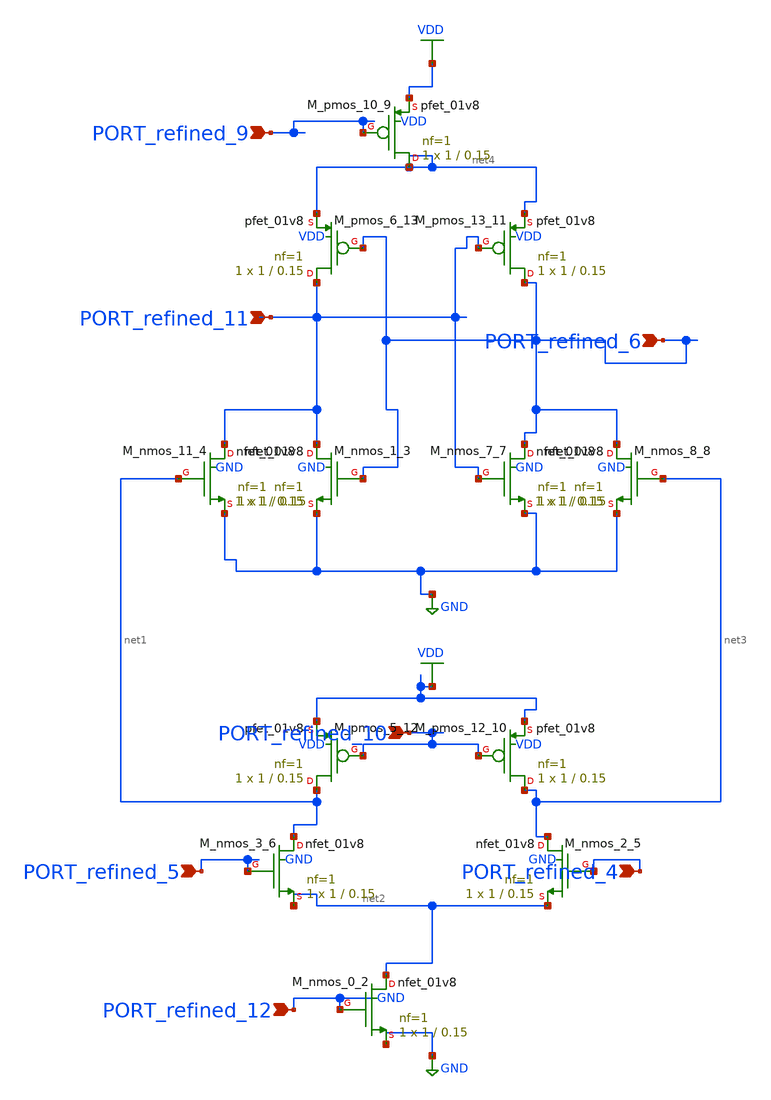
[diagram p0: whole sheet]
** sch_path: schematics/10_1109_ACCESS_2019_2927514_02_002.sch
**.subckt 10_1109_ACCESS_2019_2927514_02_002 PORT_refined_4 PORT_refined_11 PORT_refined_12
*+ PORT_refined_5 PORT_refined_9 PORT_refined_10 PORT_refined_6
*.ipin PORT_refined_4
*.ipin PORT_refined_11
*.ipin PORT_refined_12
*.ipin PORT_refined_5
*.ipin PORT_refined_9
*.ipin PORT_refined_10
*.ipin PORT_refined_6
XM_nmos_0_2 net2 PORT_refined_12 GND GND sky130_fd_pr__nfet_01v8 L=0.15 W=1 nf=1 ad='int((1 + 1)/2) * 1 / 1 * 0.29'
+ as='int((1 + 2)/2) * 1 / 1 * 0.29' pd='2*int((1 + 1)/2) * (1 / 1 + 0.29)' ps='2*int((1 + 2)/2) * (1 / 1 + 0.29)'
+ nrd='0.29 / 1 ' nrs='0.29 / 1 ' sa=0 sb=0 sd=0 mult=1 m=1
XM_nmos_1_3 PORT_refined_11 PORT_refined_6 GND GND sky130_fd_pr__nfet_01v8 L=0.15 W=1 nf=1 ad='int((1 + 1)/2) * 1 / 1 * 0.29'
+ as='int((1 + 2)/2) * 1 / 1 * 0.29' pd='2*int((1 + 1)/2) * (1 / 1 + 0.29)' ps='2*int((1 + 2)/2) * (1 / 1 + 0.29)'
+ nrd='0.29 / 1 ' nrs='0.29 / 1 ' sa=0 sb=0 sd=0 mult=1 m=1
XM_nmos_11_4 PORT_refined_11 net1 GND GND sky130_fd_pr__nfet_01v8 L=0.15 W=1 nf=1 ad='int((1 + 1)/2) * 1 / 1 * 0.29'
+ as='int((1 + 2)/2) * 1 / 1 * 0.29' pd='2*int((1 + 1)/2) * (1 / 1 + 0.29)' ps='2*int((1 + 2)/2) * (1 / 1 + 0.29)'
+ nrd='0.29 / 1 ' nrs='0.29 / 1 ' sa=0 sb=0 sd=0 mult=1 m=1
XM_nmos_2_5 net3 PORT_refined_4 net2 GND sky130_fd_pr__nfet_01v8 L=0.15 W=1 nf=1 ad='int((1 + 1)/2) * 1 / 1 * 0.29'
+ as='int((1 + 2)/2) * 1 / 1 * 0.29' pd='2*int((1 + 1)/2) * (1 / 1 + 0.29)' ps='2*int((1 + 2)/2) * (1 / 1 + 0.29)'
+ nrd='0.29 / 1 ' nrs='0.29 / 1 ' sa=0 sb=0 sd=0 mult=1 m=1
XM_nmos_3_6 net1 PORT_refined_5 net2 GND sky130_fd_pr__nfet_01v8 L=0.15 W=1 nf=1 ad='int((1 + 1)/2) * 1 / 1 * 0.29'
+ as='int((1 + 2)/2) * 1 / 1 * 0.29' pd='2*int((1 + 1)/2) * (1 / 1 + 0.29)' ps='2*int((1 + 2)/2) * (1 / 1 + 0.29)'
+ nrd='0.29 / 1 ' nrs='0.29 / 1 ' sa=0 sb=0 sd=0 mult=1 m=1
XM_nmos_7_7 PORT_refined_6 PORT_refined_11 GND GND sky130_fd_pr__nfet_01v8 L=0.15 W=1 nf=1 ad='int((1 + 1)/2) * 1 / 1 * 0.29'
+ as='int((1 + 2)/2) * 1 / 1 * 0.29' pd='2*int((1 + 1)/2) * (1 / 1 + 0.29)' ps='2*int((1 + 2)/2) * (1 / 1 + 0.29)'
+ nrd='0.29 / 1 ' nrs='0.29 / 1 ' sa=0 sb=0 sd=0 mult=1 m=1
XM_nmos_8_8 PORT_refined_6 net3 GND GND sky130_fd_pr__nfet_01v8 L=0.15 W=1 nf=1 ad='int((1 + 1)/2) * 1 / 1 * 0.29'
+ as='int((1 + 2)/2) * 1 / 1 * 0.29' pd='2*int((1 + 1)/2) * (1 / 1 + 0.29)' ps='2*int((1 + 2)/2) * (1 / 1 + 0.29)'
+ nrd='0.29 / 1 ' nrs='0.29 / 1 ' sa=0 sb=0 sd=0 mult=1 m=1
XM_pmos_10_9 net4 PORT_refined_9 VDD VDD sky130_fd_pr__pfet_01v8 L=0.15 W=1 nf=1 ad='int((1 + 1)/2) * 1 / 1 * 0.29'
+ as='int((1 + 2)/2) * 1 / 1 * 0.29' pd='2*int((1 + 1)/2) * (1 / 1 + 0.29)' ps='2*int((1 + 2)/2) * (1 / 1 + 0.29)'
+ nrd='0.29 / 1 ' nrs='0.29 / 1 ' sa=0 sb=0 sd=0 mult=1 m=1
XM_pmos_12_10 net3 PORT_refined_10 VDD VDD sky130_fd_pr__pfet_01v8 L=0.15 W=1 nf=1 ad='int((1 + 1)/2) * 1 / 1 * 0.29'
+ as='int((1 + 2)/2) * 1 / 1 * 0.29' pd='2*int((1 + 1)/2) * (1 / 1 + 0.29)' ps='2*int((1 + 2)/2) * (1 / 1 + 0.29)'
+ nrd='0.29 / 1 ' nrs='0.29 / 1 ' sa=0 sb=0 sd=0 mult=1 m=1
XM_pmos_13_11 PORT_refined_6 PORT_refined_11 net4 VDD sky130_fd_pr__pfet_01v8 L=0.15 W=1 nf=1 ad='int((1 + 1)/2) * 1 / 1 * 0.29'
+ as='int((1 + 2)/2) * 1 / 1 * 0.29' pd='2*int((1 + 1)/2) * (1 / 1 + 0.29)' ps='2*int((1 + 2)/2) * (1 / 1 + 0.29)'
+ nrd='0.29 / 1 ' nrs='0.29 / 1 ' sa=0 sb=0 sd=0 mult=1 m=1
XM_pmos_5_12 net1 PORT_refined_10 VDD VDD sky130_fd_pr__pfet_01v8 L=0.15 W=1 nf=1 ad='int((1 + 1)/2) * 1 / 1 * 0.29'
+ as='int((1 + 2)/2) * 1 / 1 * 0.29' pd='2*int((1 + 1)/2) * (1 / 1 + 0.29)' ps='2*int((1 + 2)/2) * (1 / 1 + 0.29)'
+ nrd='0.29 / 1 ' nrs='0.29 / 1 ' sa=0 sb=0 sd=0 mult=1 m=1
XM_pmos_6_13 PORT_refined_11 PORT_refined_6 net4 VDD sky130_fd_pr__pfet_01v8 L=0.15 W=1 nf=1 ad='int((1 + 1)/2) * 1 / 1 * 0.29'
+ as='int((1 + 2)/2) * 1 / 1 * 0.29' pd='2*int((1 + 1)/2) * (1 / 1 + 0.29)' ps='2*int((1 + 2)/2) * (1 / 1 + 0.29)'
+ nrd='0.29 / 1 ' nrs='0.29 / 1 ' sa=0 sb=0 sd=0 mult=1 m=1
**.ends
.GLOBAL GND
.GLOBAL VDD
.end
